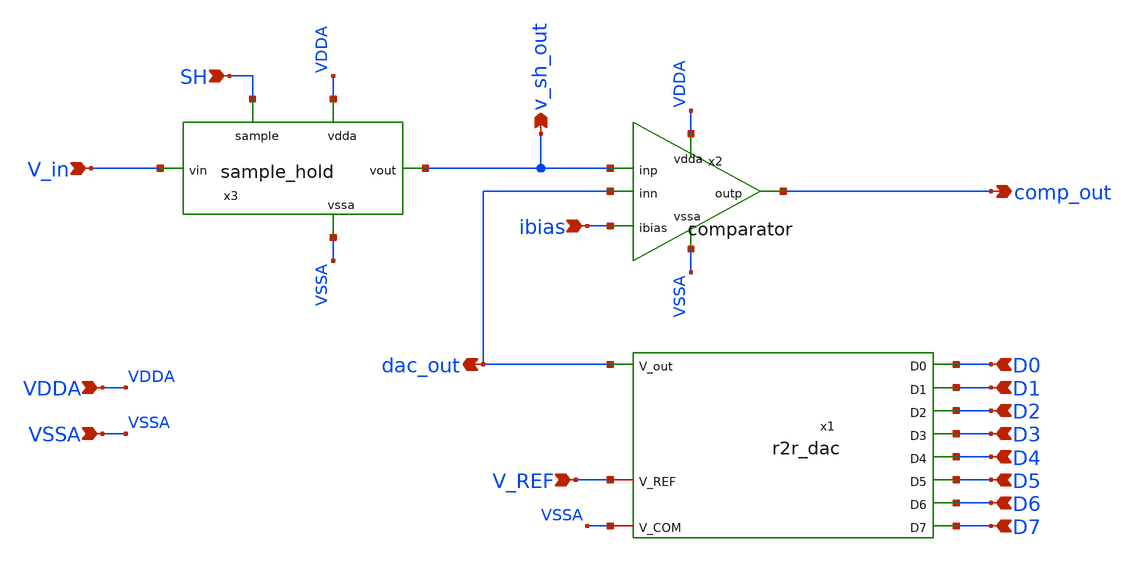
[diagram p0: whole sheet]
** sch_path: xschem/sar_adc_analog.sch
**.subckt sar_adc_analog D0 comp_out D1 D2 D3 D4 D5 D6 D7 V_REF SH V_in VDDA VSSA ibias dac_out
*+ v_sh_out
*.ipin D0
*.opin comp_out
*.ipin D1
*.ipin D2
*.ipin D3
*.ipin D4
*.ipin D5
*.ipin D6
*.ipin D7
*.ipin V_REF
*.ipin SH
*.ipin V_in
*.ipin VDDA
*.ipin VSSA
*.ipin ibias
*.opin dac_out
*.opin v_sh_out
x1 dac_out D7 D0 D1 D6 D2 D5 D3 D4 V_REF VSSA r2r_dac
x2 VDDA ibias v_sh_out dac_out comp_out VSSA comparator
x3 VDDA SH v_sh_out V_in VSSA sample_hold
**.ends
.end
